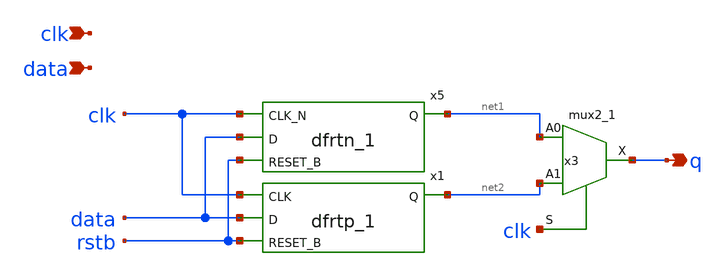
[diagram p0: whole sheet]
** sch_path: xschem/tryandtest/deff.sch
**.subckt deff clk data q
*.ipin clk
*.ipin data
*.opin q
x3 net1 net2 clk GND GND VDD VDD q sky130_fd_sc_lp__mux2_1
x5 clk data rstb GND GND VDD VDD net1 sky130_fd_sc_lp__dfrtn_1
x1 clk data rstb GND GND VDD VDD net2 sky130_fd_sc_lp__dfrtp_1
**.ends
.end
